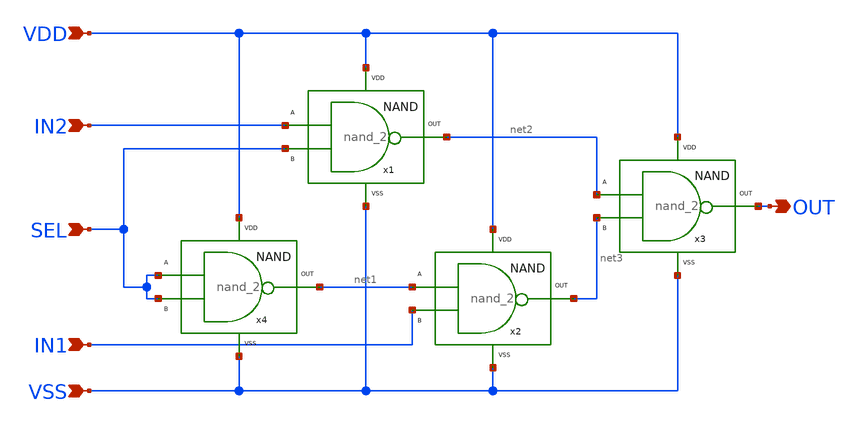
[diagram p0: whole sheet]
** sch_path: designs/libs/PNgen/mux2_1.sch
**.subckt mux2_1 VDD VSS IN2 IN1 SEL OUT
*.ipin VDD
*.ipin VSS
*.ipin IN2
*.ipin IN1
*.ipin SEL
*.opin OUT
x1 IN2 SEL VDD VSS net2 nand_2
x2 net1 IN1 VDD VSS net3 nand_2
x3 net2 net3 VDD VSS OUT nand_2
x4 SEL SEL VDD VSS net1 nand_2
**.ends

* expanding   symbol:  prof-morbius-rf-chip/designs/libs/PNgen/nand_2.sym # of pins=5
** sym_path: prof-morbius-rf-chip/designs/libs/PNgen/nand_2.sym
** sch_path: prof-morbius-rf-chip/designs/libs/PNgen/nand_2.sch
.subckt nand_2 A B VDD VSS OUT
*.ipin VDD
*.opin OUT
*.ipin A
*.ipin B
*.ipin VSS
XM1 OUT A net1 VSS nfet_03v3 L=0.28u W=1.2u nf=1 ad='int((nf+1)/2) * W/nf * 0.18u' as='int((nf+2)/2) * W/nf * 0.18u'
+ pd='2*int((nf+1)/2) * (W/nf + 0.18u)' ps='2*int((nf+2)/2) * (W/nf + 0.18u)' nrd='0.18u / W' nrs='0.18u / W'
+ sa=0 sb=0 sd=0 m=1
XM2 OUT A VDD VDD pfet_03v3 L=0.28u W=1.3u nf=1 ad='int((nf+1)/2) * W/nf * 0.18u' as='int((nf+2)/2) * W/nf * 0.18u'
+ pd='2*int((nf+1)/2) * (W/nf + 0.18u)' ps='2*int((nf+2)/2) * (W/nf + 0.18u)' nrd='0.18u / W' nrs='0.18u / W'
+ sa=0 sb=0 sd=0 m=1
XM3 OUT B VDD VDD pfet_03v3 L=0.28u W=1.3u nf=1 ad='int((nf+1)/2) * W/nf * 0.18u' as='int((nf+2)/2) * W/nf * 0.18u'
+ pd='2*int((nf+1)/2) * (W/nf + 0.18u)' ps='2*int((nf+2)/2) * (W/nf + 0.18u)' nrd='0.18u / W' nrs='0.18u / W'
+ sa=0 sb=0 sd=0 m=1
XM4 net1 B VSS VSS nfet_03v3 L=0.28u W=1.2u nf=1 ad='int((nf+1)/2) * W/nf * 0.18u' as='int((nf+2)/2) * W/nf * 0.18u'
+ pd='2*int((nf+1)/2) * (W/nf + 0.18u)' ps='2*int((nf+2)/2) * (W/nf + 0.18u)' nrd='0.18u / W' nrs='0.18u / W'
+ sa=0 sb=0 sd=0 m=1
.ends

.end
